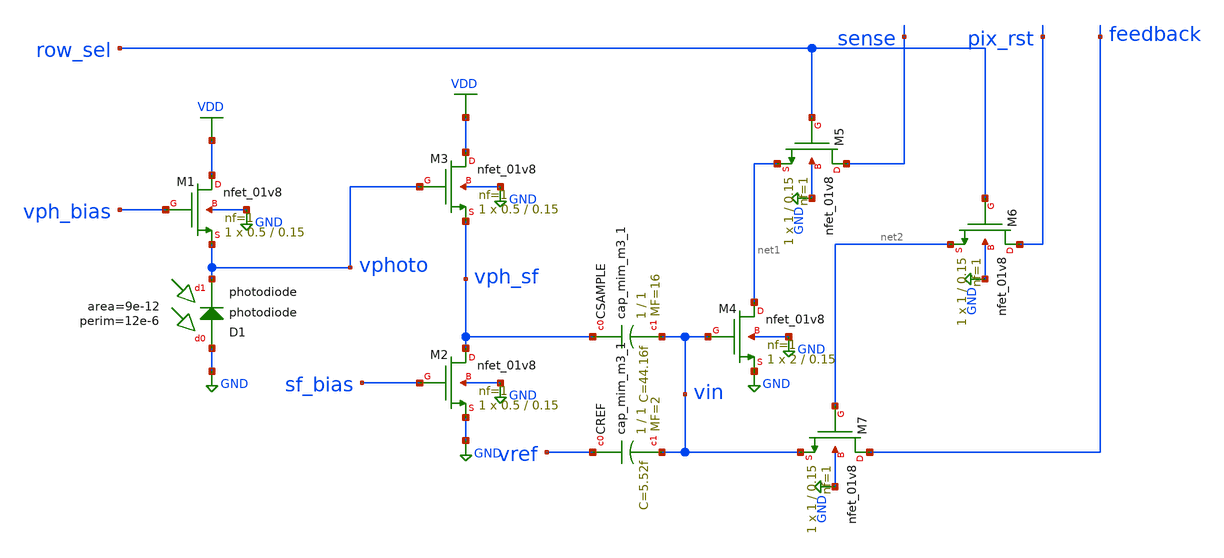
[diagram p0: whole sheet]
** sch_path: analog/xschem/openDVS_pixel.sch
**.subckt openDVS_pixel
XCSAMPLE vph_sf vin sky130_fd_pr__cap_mim_m3_1 W=1 L=1 MF=16 m=16
XCREF vref vin sky130_fd_pr__cap_mim_m3_1 W=1 L=1 MF=2 m=2
XM1 VDD vph_bias vphoto GND sky130_fd_pr__nfet_01v8 L=0.15 W=0.5 nf=1 ad='int((1 + 1)/2) * 0.5 / 1 * 0.29'
+ as='int((1 + 2)/2) * 0.5 / 1 * 0.29' pd='2*int((1 + 1)/2) * (0.5 / 1 + 0.29)' ps='2*int((1 + 2)/2) * (0.5 / 1 + 0.29)'
+ nrd='0.29 / 0.5 ' nrs='0.29 / 0.5 ' sa=0 sb=0 sd=0 mult=1 m=1
XM4 net1 vin GND GND sky130_fd_pr__nfet_01v8 L=0.15 W=2 nf=1 ad='int((1 + 1)/2) * 2 / 1 * 0.29' as='int((1 + 2)/2) * 2 / 1 * 0.29'
+ pd='2*int((1 + 1)/2) * (2 / 1 + 0.29)' ps='2*int((1 + 2)/2) * (2 / 1 + 0.29)' nrd='0.29 / 2 ' nrs='0.29 / 2 '
+ sa=0 sb=0 sd=0 mult=1 m=1
XM7 feedback net2 vin GND sky130_fd_pr__nfet_01v8 L=0.15 W=1 nf=1 ad='int((1 + 1)/2) * 1 / 1 * 0.29'
+ as='int((1 + 2)/2) * 1 / 1 * 0.29' pd='2*int((1 + 1)/2) * (1 / 1 + 0.29)' ps='2*int((1 + 2)/2) * (1 / 1 + 0.29)'
+ nrd='0.29 / 1 ' nrs='0.29 / 1 ' sa=0 sb=0 sd=0 mult=1 m=1
XM2 vph_sf sf_bias GND GND sky130_fd_pr__nfet_01v8 L=0.15 W=0.5 nf=1 ad='int((1 + 1)/2) * 0.5 / 1 * 0.29'
+ as='int((1 + 2)/2) * 0.5 / 1 * 0.29' pd='2*int((1 + 1)/2) * (0.5 / 1 + 0.29)' ps='2*int((1 + 2)/2) * (0.5 / 1 + 0.29)'
+ nrd='0.29 / 0.5 ' nrs='0.29 / 0.5 ' sa=0 sb=0 sd=0 mult=1 m=1
XM3 VDD vphoto vph_sf GND sky130_fd_pr__nfet_01v8 L=0.15 W=0.5 nf=1 ad='int((1 + 1)/2) * 0.5 / 1 * 0.29'
+ as='int((1 + 2)/2) * 0.5 / 1 * 0.29' pd='2*int((1 + 1)/2) * (0.5 / 1 + 0.29)' ps='2*int((1 + 2)/2) * (0.5 / 1 + 0.29)'
+ nrd='0.29 / 0.5 ' nrs='0.29 / 0.5 ' sa=0 sb=0 sd=0 mult=1 m=1
XD1 GND vphoto sky130_fd_pr__photodiode area=9e-12 perim=12e-6
XM5 sense row_sel net1 GND sky130_fd_pr__nfet_01v8 L=0.15 W=1 nf=1 ad='int((1 + 1)/2) * 1 / 1 * 0.29'
+ as='int((1 + 2)/2) * 1 / 1 * 0.29' pd='2*int((1 + 1)/2) * (1 / 1 + 0.29)' ps='2*int((1 + 2)/2) * (1 / 1 + 0.29)'
+ nrd='0.29 / 1 ' nrs='0.29 / 1 ' sa=0 sb=0 sd=0 mult=1 m=1
XM6 pix_rst row_sel net2 GND sky130_fd_pr__nfet_01v8 L=0.15 W=1 nf=1 ad='int((1 + 1)/2) * 1 / 1 * 0.29'
+ as='int((1 + 2)/2) * 1 / 1 * 0.29' pd='2*int((1 + 1)/2) * (1 / 1 + 0.29)' ps='2*int((1 + 2)/2) * (1 / 1 + 0.29)'
+ nrd='0.29 / 1 ' nrs='0.29 / 1 ' sa=0 sb=0 sd=0 mult=1 m=1
**.ends
.GLOBAL VDD
.GLOBAL GND
.end
